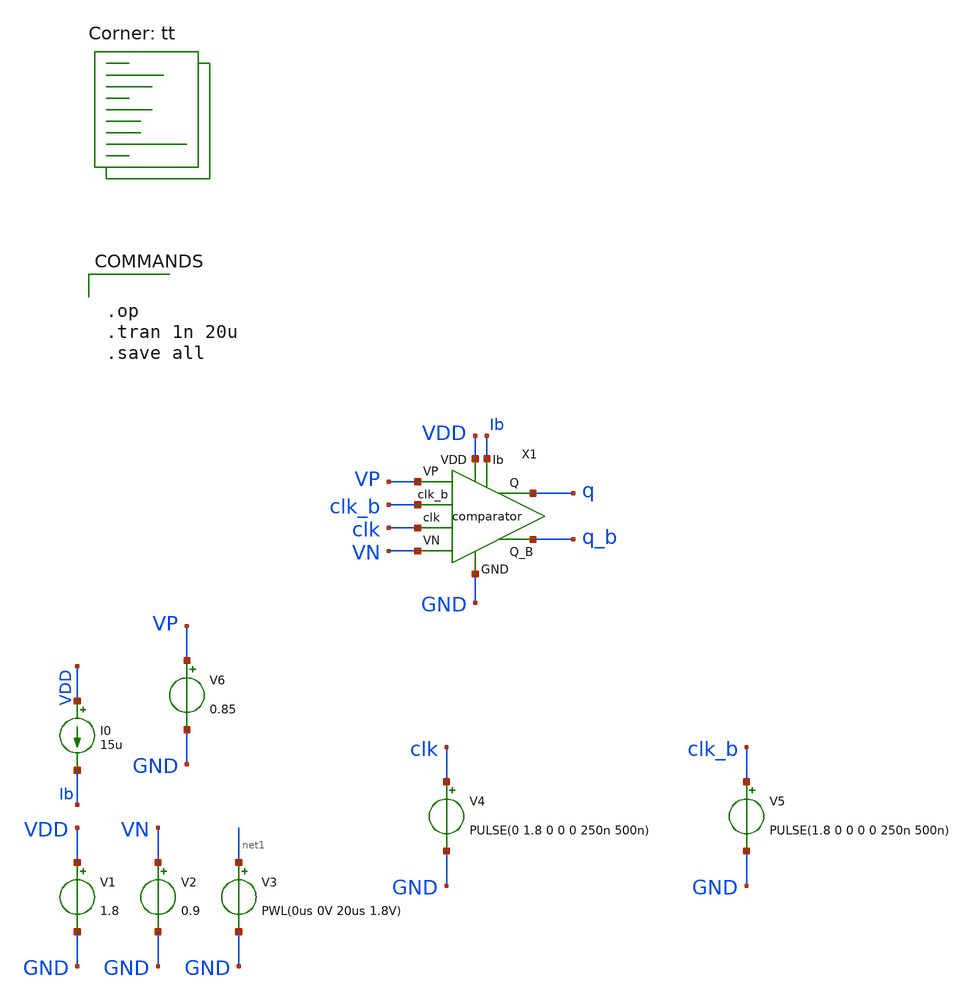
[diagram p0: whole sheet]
** sch_path: xschem/comparator/comparator_tb.sch
**.subckt comparator_tb
V1 VDD GND 1.8
V2 VN GND 0.9
V3 net1 GND PWL(0us 0V 20us 1.8V)
V4 clk GND PULSE(0 1.8 0 0 0 250n 500n)
I0 VDD Ib 15u
V5 clk_b GND PULSE(1.8 0 0 0 0 250n 500n)
X1 VP VN GND q_b q VDD clk Ib clk_b comparator
V6 VP GND 0.85
**** begin user architecture code
.lib $::SKYWATER_MODELS/sky130.lib.spice tt


.op
.tran 1n 20u
.save all


**** end user architecture code
**.ends
.end
